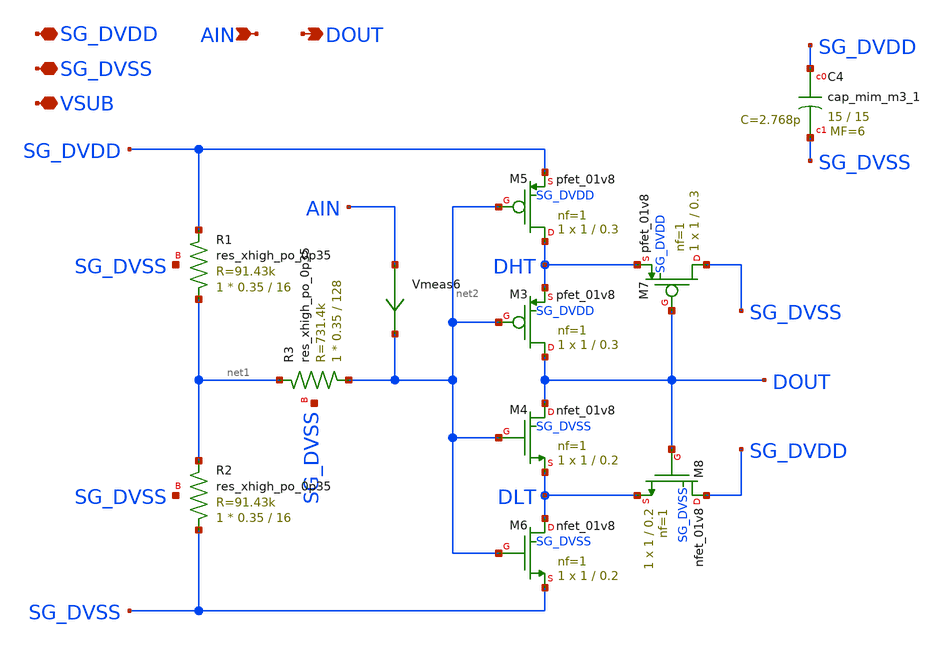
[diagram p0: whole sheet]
** sch_path: xschem/schmitt_trigger_pullmid.sch
**.subckt schmitt_trigger_pullmid SG_DVDD SG_DVSS AIN DOUT VSUB
*.iopin SG_DVDD
*.iopin SG_DVSS
*.ipin AIN
*.opin DOUT
*.iopin VSUB
XR3 net2 net1 SG_DVSS sky130_fd_pr__res_xhigh_po_0p35 L=128 mult=1 m=1
XM3 DOUT net2 DHT SG_DVDD sky130_fd_pr__pfet_01v8 L=0.3 W=1 nf=1 ad='int((1 + 1)/2) * 1 / 1 * 0.29' as='int((1 + 2)/2) * 1 / 1 * 0.29'
+ pd='2*int((1 + 1)/2) * (1 / 1 + 0.29)' ps='2*int((1 + 2)/2) * (1 / 1 + 0.29)' nrd='0.29 / 1 ' nrs='0.29 / 1 '
+ sa=0 sb=0 sd=0 mult=1 m=1
XM4 DOUT net2 DLT SG_DVSS sky130_fd_pr__nfet_01v8 L=0.2 W=1 nf=1 ad='int((nf+1)/2) * W/nf * 0.29' as='int((nf+2)/2) * W/nf * 0.29'
+ pd='2*int((nf+1)/2) * (W/nf + 0.29)' ps='2*int((nf+2)/2) * (W/nf + 0.29)' nrd='0.29 / W' nrs='0.29 / W'
+ sa=0 sb=0 sd=0 mult=1 m=1
XM5 DHT net2 SG_DVDD SG_DVDD sky130_fd_pr__pfet_01v8 L=0.3 W=1 nf=1 ad='int((1 + 1)/2) * 1 / 1 * 0.29'
+ as='int((1 + 2)/2) * 1 / 1 * 0.29' pd='2*int((1 + 1)/2) * (1 / 1 + 0.29)' ps='2*int((1 + 2)/2) * (1 / 1 + 0.29)'
+ nrd='0.29 / 1 ' nrs='0.29 / 1 ' sa=0 sb=0 sd=0 mult=1 m=1
XM6 DLT net2 SG_DVSS SG_DVSS sky130_fd_pr__nfet_01v8 L=0.2 W=1 nf=1 ad='int((nf+1)/2) * W/nf * 0.29'
+ as='int((nf+2)/2) * W/nf * 0.29' pd='2*int((nf+1)/2) * (W/nf + 0.29)' ps='2*int((nf+2)/2) * (W/nf + 0.29)'
+ nrd='0.29 / W' nrs='0.29 / W' sa=0 sb=0 sd=0 mult=1 m=1
XM7 SG_DVSS DOUT DHT SG_DVDD sky130_fd_pr__pfet_01v8 L=0.3 W=1 nf=1 ad='int((1 + 1)/2) * 1 / 1 * 0.29'
+ as='int((1 + 2)/2) * 1 / 1 * 0.29' pd='2*int((1 + 1)/2) * (1 / 1 + 0.29)' ps='2*int((1 + 2)/2) * (1 / 1 + 0.29)'
+ nrd='0.29 / 1 ' nrs='0.29 / 1 ' sa=0 sb=0 sd=0 mult=1 m=1
XM8 SG_DVDD DOUT DLT SG_DVSS sky130_fd_pr__nfet_01v8 L=0.2 W=1 nf=1 ad='int((nf+1)/2) * W/nf * 0.29'
+ as='int((nf+2)/2) * W/nf * 0.29' pd='2*int((nf+1)/2) * (W/nf + 0.29)' ps='2*int((nf+2)/2) * (W/nf + 0.29)'
+ nrd='0.29 / W' nrs='0.29 / W' sa=0 sb=0 sd=0 mult=1 m=1
XC4 SG_DVDD SG_DVSS sky130_fd_pr__cap_mim_m3_1 W=15 L=15 MF=6 m=6
XR1 net1 SG_DVDD SG_DVSS sky130_fd_pr__res_xhigh_po_0p35 L=16 mult=1 m=1
XR2 SG_DVSS net1 SG_DVSS sky130_fd_pr__res_xhigh_po_0p35 L=16 mult=1 m=1
Vmeas6 AIN net2 0
.save i(vmeas6)
**.ends
.end
